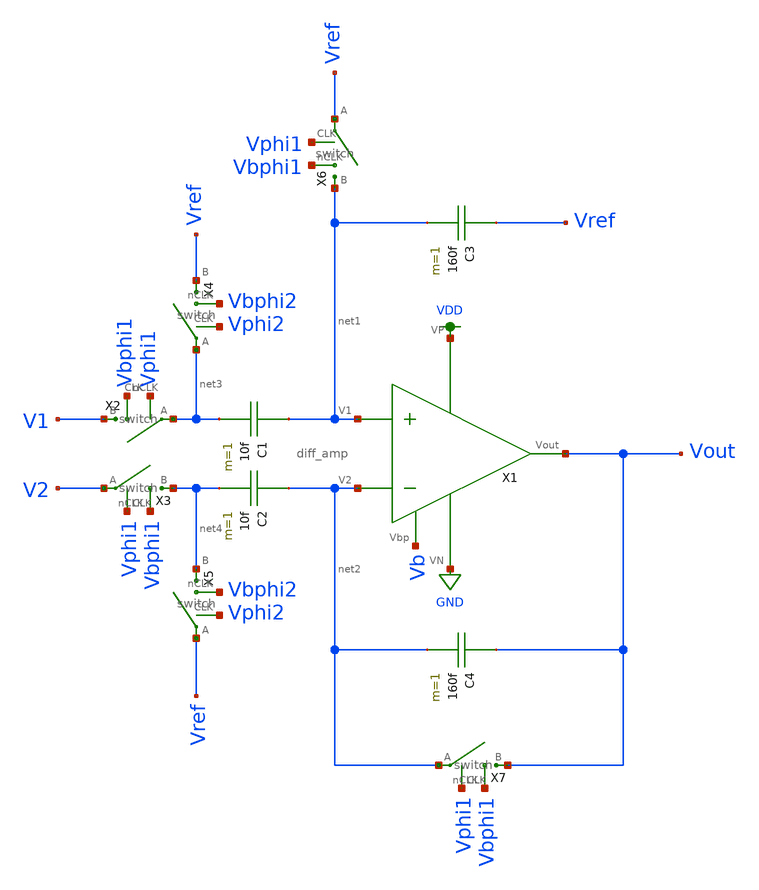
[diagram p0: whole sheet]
** sch_path: schematic/alpha_amp_new.sch
**.subckt alpha_amp_new
X1 VDD Vb Vout net1 net2 GND diff_amp
C1 net1 net3 10f m=1
C2 net2 net4 10f m=1
C3 Vref net1 160f m=1
C4 Vout net2 160f m=1
X2 V1 net3 Vphi1 Vbphi1 switch
X3 net4 V2 Vphi1 Vbphi1 switch
X4 Vref net3 Vphi2 Vbphi2 switch
X5 net4 Vref Vphi2 Vbphi2 switch
X6 net1 Vref Vphi1 Vbphi1 switch
X7 Vout net2 Vphi1 Vbphi1 switch
**.ends
.GLOBAL GND
.GLOBAL VDD
.end
